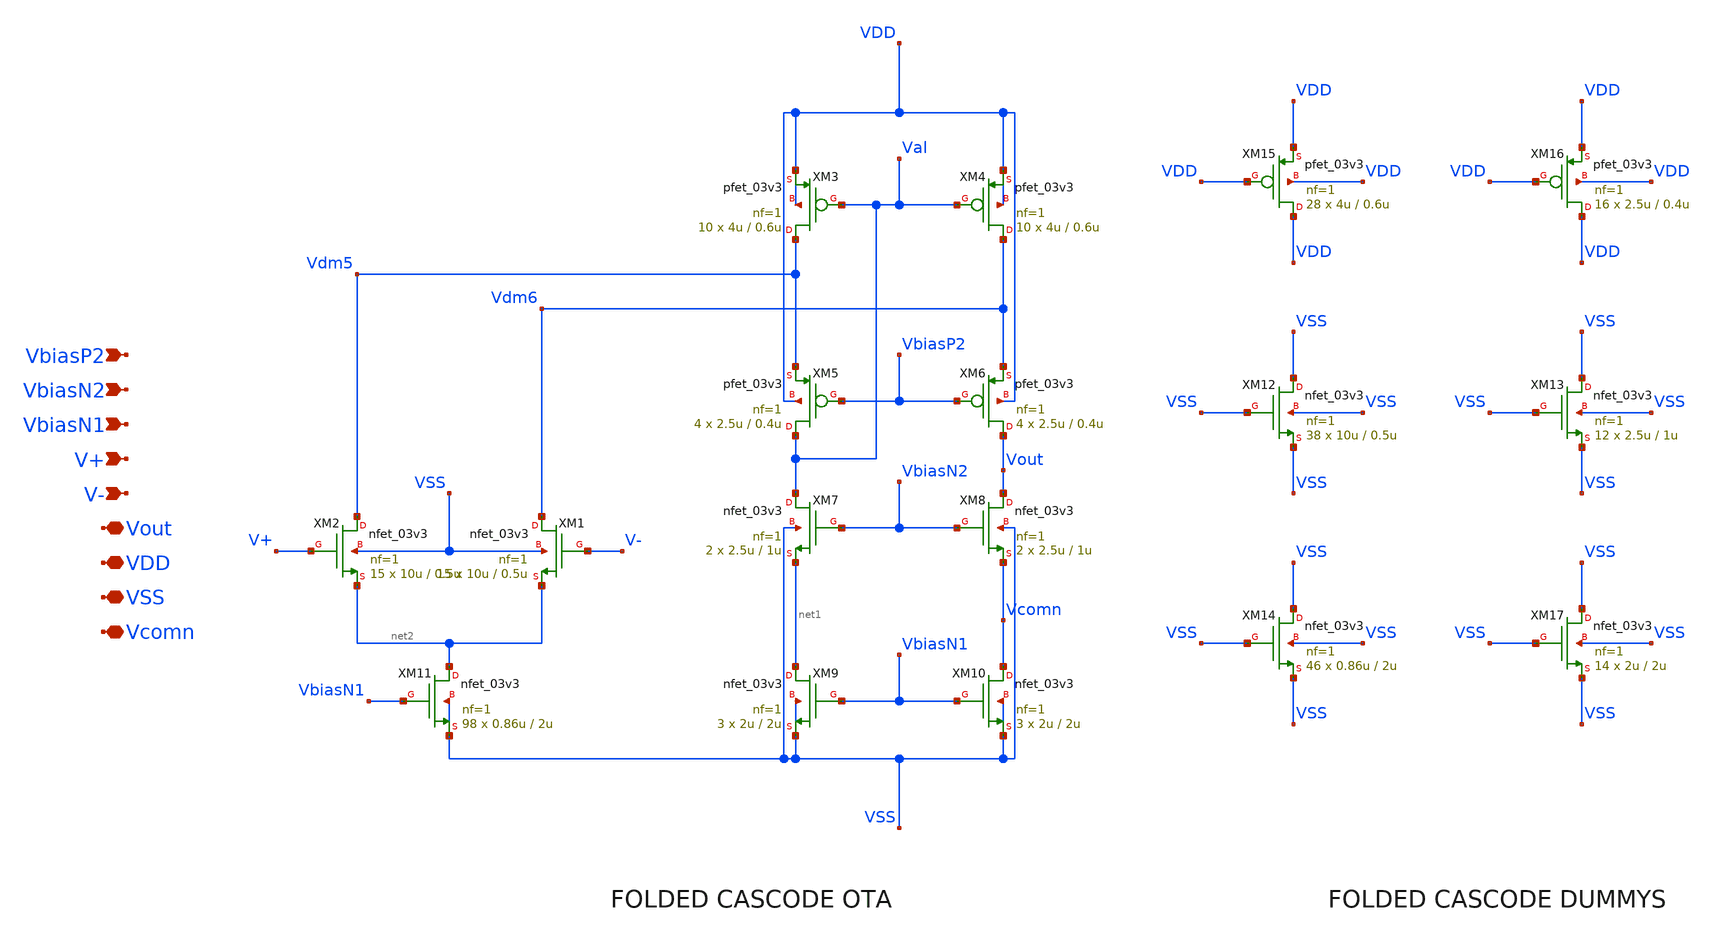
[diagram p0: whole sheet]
** sch_path: designs/gf180/error_amplifier_N_input_core_v1/xschem/error_amplifier_N_input_core_v1.sch
**.subckt error_amplifier_N_input_core_v1 VbiasN2 VDD VbiasP2 VbiasN1 V+ V- VSS Vcomn Vout
*.ipin VbiasN2
*.iopin VDD
*.ipin VbiasP2
*.ipin VbiasN1
*.ipin V+
*.ipin V-
*.iopin VSS
*.iopin Vcomn
*.iopin Vout
XM4 Vdm6 Val VDD VDD pfet_03v3 L=0.6u W=4u nf=1 ad='int((nf+1)/2) * W/nf * 0.18u' as='int((nf+2)/2) * W/nf * 0.18u'
+ pd='2*int((nf+1)/2) * (W/nf + 0.18u)' ps='2*int((nf+2)/2) * (W/nf + 0.18u)' nrd='0.18u / W' nrs='0.18u / W'
+ sa=0 sb=0 sd=0 m=10
XM3 Vdm5 Val VDD VDD pfet_03v3 L=0.6u W=4u nf=1 ad='int((nf+1)/2) * W/nf * 0.18u' as='int((nf+2)/2) * W/nf * 0.18u'
+ pd='2*int((nf+1)/2) * (W/nf + 0.18u)' ps='2*int((nf+2)/2) * (W/nf + 0.18u)' nrd='0.18u / W' nrs='0.18u / W'
+ sa=0 sb=0 sd=0 m=10
XM5 Val VbiasP2 Vdm5 VDD pfet_03v3 L=0.4u W=2.5u nf=1 ad='int((nf+1)/2) * W/nf * 0.18u' as='int((nf+2)/2) * W/nf * 0.18u'
+ pd='2*int((nf+1)/2) * (W/nf + 0.18u)' ps='2*int((nf+2)/2) * (W/nf + 0.18u)' nrd='0.18u / W' nrs='0.18u / W'
+ sa=0 sb=0 sd=0 m=4
XM6 Vout VbiasP2 Vdm6 VDD pfet_03v3 L=0.4u W=2.5u nf=1 ad='int((nf+1)/2) * W/nf * 0.18u' as='int((nf+2)/2) * W/nf * 0.18u'
+ pd='2*int((nf+1)/2) * (W/nf + 0.18u)' ps='2*int((nf+2)/2) * (W/nf + 0.18u)' nrd='0.18u / W' nrs='0.18u / W'
+ sa=0 sb=0 sd=0 m=4
XM9 net1 VbiasN1 VSS VSS nfet_03v3 L=2u W=2u nf=1 ad='int((nf+1)/2) * W/nf * 0.18u' as='int((nf+2)/2) * W/nf * 0.18u'
+ pd='2*int((nf+1)/2) * (W/nf + 0.18u)' ps='2*int((nf+2)/2) * (W/nf + 0.18u)' nrd='0.18u / W' nrs='0.18u / W'
+ sa=0 sb=0 sd=0 m=3
XM8 Vout VbiasN2 Vcomn VSS nfet_03v3 L=1u W=2.5u nf=1 ad='int((nf+1)/2) * W/nf * 0.18u' as='int((nf+2)/2) * W/nf * 0.18u'
+ pd='2*int((nf+1)/2) * (W/nf + 0.18u)' ps='2*int((nf+2)/2) * (W/nf + 0.18u)' nrd='0.18u / W' nrs='0.18u / W'
+ sa=0 sb=0 sd=0 m=2
XM7 Val VbiasN2 net1 VSS nfet_03v3 L=1u W=2.5u nf=1 ad='int((nf+1)/2) * W/nf * 0.18u' as='int((nf+2)/2) * W/nf * 0.18u'
+ pd='2*int((nf+1)/2) * (W/nf + 0.18u)' ps='2*int((nf+2)/2) * (W/nf + 0.18u)' nrd='0.18u / W' nrs='0.18u / W'
+ sa=0 sb=0 sd=0 m=2
XM10 Vcomn VbiasN1 VSS VSS nfet_03v3 L=2u W=2u nf=1 ad='int((nf+1)/2) * W/nf * 0.18u' as='int((nf+2)/2) * W/nf * 0.18u'
+ pd='2*int((nf+1)/2) * (W/nf + 0.18u)' ps='2*int((nf+2)/2) * (W/nf + 0.18u)' nrd='0.18u / W' nrs='0.18u / W'
+ sa=0 sb=0 sd=0 m=3
XM15 VDD VDD VDD VDD pfet_03v3 L=0.6u W=4u nf=1 ad='int((nf+1)/2) * W/nf * 0.18u' as='int((nf+2)/2) * W/nf * 0.18u'
+ pd='2*int((nf+1)/2) * (W/nf + 0.18u)' ps='2*int((nf+2)/2) * (W/nf + 0.18u)' nrd='0.18u / W' nrs='0.18u / W'
+ sa=0 sb=0 sd=0 m=28
XM16 VDD VDD VDD VDD pfet_03v3 L=0.4u W=2.5u nf=1 ad='int((nf+1)/2) * W/nf * 0.18u' as='int((nf+2)/2) * W/nf * 0.18u'
+ pd='2*int((nf+1)/2) * (W/nf + 0.18u)' ps='2*int((nf+2)/2) * (W/nf + 0.18u)' nrd='0.18u / W' nrs='0.18u / W'
+ sa=0 sb=0 sd=0 m=16
XM13 VSS VSS VSS VSS nfet_03v3 L=1u W=2.5u nf=1 ad='int((nf+1)/2) * W/nf * 0.18u' as='int((nf+2)/2) * W/nf * 0.18u'
+ pd='2*int((nf+1)/2) * (W/nf + 0.18u)' ps='2*int((nf+2)/2) * (W/nf + 0.18u)' nrd='0.18u / W' nrs='0.18u / W'
+ sa=0 sb=0 sd=0 m=12
XM12 VSS VSS VSS VSS nfet_03v3 L=0.5u W=10u nf=1 ad='int((nf+1)/2) * W/nf * 0.18u' as='int((nf+2)/2) * W/nf * 0.18u'
+ pd='2*int((nf+1)/2) * (W/nf + 0.18u)' ps='2*int((nf+2)/2) * (W/nf + 0.18u)' nrd='0.18u / W' nrs='0.18u / W'
+ sa=0 sb=0 sd=0 m=38
XM14 VSS VSS VSS VSS nfet_03v3 L=2u W=0.86u nf=1 ad='int((nf+1)/2) * W/nf * 0.18u' as='int((nf+2)/2) * W/nf * 0.18u'
+ pd='2*int((nf+1)/2) * (W/nf + 0.18u)' ps='2*int((nf+2)/2) * (W/nf + 0.18u)' nrd='0.18u / W' nrs='0.18u / W'
+ sa=0 sb=0 sd=0 m=46
XM1 Vdm6 V- net2 VSS nfet_03v3 L=0.5u W=10u nf=1 ad='int((nf+1)/2) * W/nf * 0.18u' as='int((nf+2)/2) * W/nf * 0.18u'
+ pd='2*int((nf+1)/2) * (W/nf + 0.18u)' ps='2*int((nf+2)/2) * (W/nf + 0.18u)' nrd='0.18u / W' nrs='0.18u / W'
+ sa=0 sb=0 sd=0 m=15
XM2 Vdm5 V+ net2 VSS nfet_03v3 L=0.5u W=10u nf=1 ad='int((nf+1)/2) * W/nf * 0.18u' as='int((nf+2)/2) * W/nf * 0.18u'
+ pd='2*int((nf+1)/2) * (W/nf + 0.18u)' ps='2*int((nf+2)/2) * (W/nf + 0.18u)' nrd='0.18u / W' nrs='0.18u / W'
+ sa=0 sb=0 sd=0 m=15
XM11 net2 VbiasN1 VSS VSS nfet_03v3 L=2u W=0.86u nf=1 ad='int((nf+1)/2) * W/nf * 0.18u' as='int((nf+2)/2) * W/nf * 0.18u'
+ pd='2*int((nf+1)/2) * (W/nf + 0.18u)' ps='2*int((nf+2)/2) * (W/nf + 0.18u)' nrd='0.18u / W' nrs='0.18u / W'
+ sa=0 sb=0 sd=0 m=98
XM17 VSS VSS VSS VSS nfet_03v3 L=2u W=2u nf=1 ad='int((nf+1)/2) * W/nf * 0.18u' as='int((nf+2)/2) * W/nf * 0.18u'
+ pd='2*int((nf+1)/2) * (W/nf + 0.18u)' ps='2*int((nf+2)/2) * (W/nf + 0.18u)' nrd='0.18u / W' nrs='0.18u / W'
+ sa=0 sb=0 sd=0 m=14
**.ends
.end
